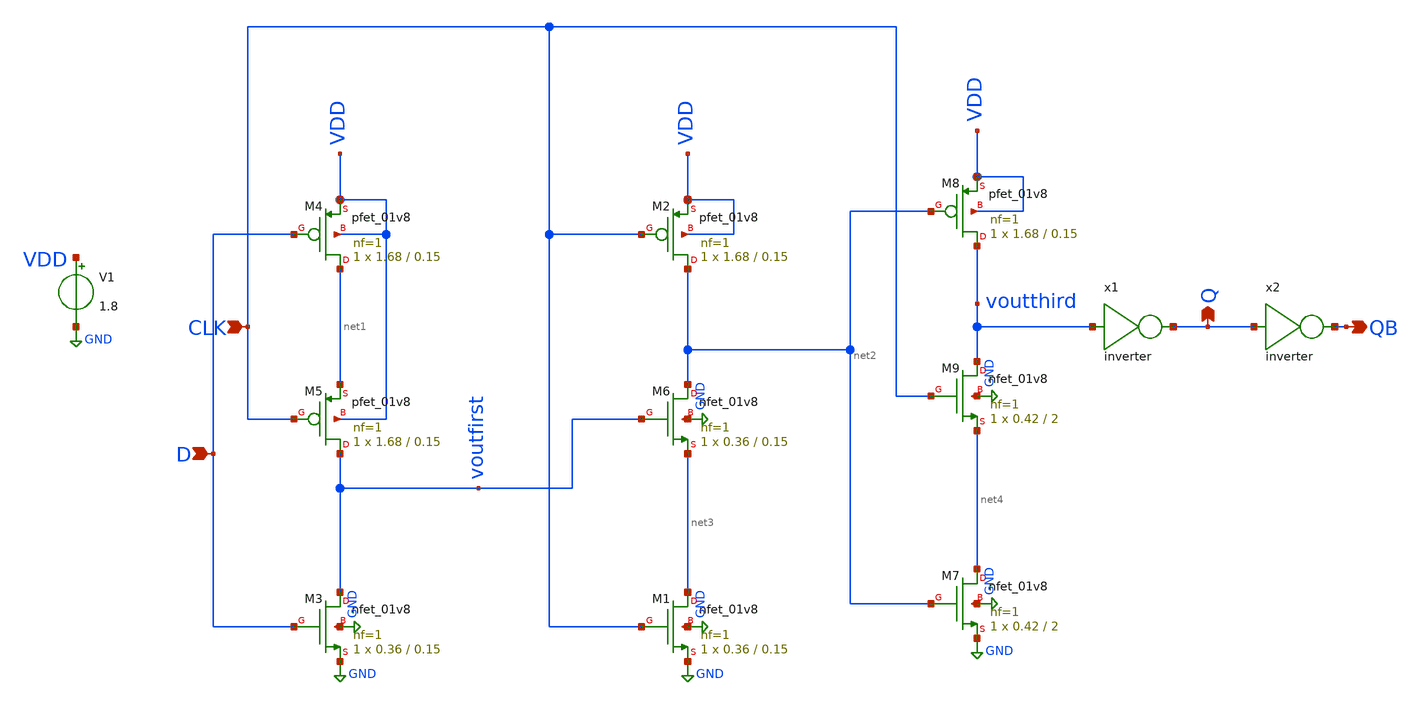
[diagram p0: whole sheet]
** sch_path: TSPC_Dff.sch
**.subckt TSPC_Dff D CLK Q QB
*.ipin D
*.ipin CLK
*.opin Q
*.opin QB
V1 VDD GND 1.8
XM3 voutfirst D GND GND sky130_fd_pr__nfet_01v8 L=0.15 W=0.36 nf=1 ad='int((nf+1)/2) * W/nf * 0.29' as='int((nf+2)/2) * W/nf * 0.29'
+ pd='2*int((nf+1)/2) * (W/nf + 0.29)' ps='2*int((nf+2)/2) * (W/nf + 0.29)' nrd='0.29 / W' nrs='0.29 / W'
+ sa=0 sb=0 sd=0 mult=1 m=1
XM4 net1 D VDD VDD sky130_fd_pr__pfet_01v8 L=0.15 W=1.68 nf=1 ad='int((nf+1)/2) * W/nf * 0.29' as='int((nf+2)/2) * W/nf * 0.29'
+ pd='2*int((nf+1)/2) * (W/nf + 0.29)' ps='2*int((nf+2)/2) * (W/nf + 0.29)' nrd='0.29 / W' nrs='0.29 / W'
+ sa=0 sb=0 sd=0 mult=1 m=1
XM5 voutfirst CLK net1 VDD sky130_fd_pr__pfet_01v8 L=0.15 W=1.68 nf=1 ad='int((nf+1)/2) * W/nf * 0.29'
+ as='int((nf+2)/2) * W/nf * 0.29' pd='2*int((nf+1)/2) * (W/nf + 0.29)' ps='2*int((nf+2)/2) * (W/nf + 0.29)'
+ nrd='0.29 / W' nrs='0.29 / W' sa=0 sb=0 sd=0 mult=1 m=1
XM1 net3 CLK GND GND sky130_fd_pr__nfet_01v8 L=0.15 W=0.36 nf=1 ad='int((nf+1)/2) * W/nf * 0.29' as='int((nf+2)/2) * W/nf * 0.29'
+ pd='2*int((nf+1)/2) * (W/nf + 0.29)' ps='2*int((nf+2)/2) * (W/nf + 0.29)' nrd='0.29 / W' nrs='0.29 / W'
+ sa=0 sb=0 sd=0 mult=1 m=1
XM2 net2 CLK VDD VDD sky130_fd_pr__pfet_01v8 L=0.15 W=1.68 nf=1 ad='int((nf+1)/2) * W/nf * 0.29' as='int((nf+2)/2) * W/nf * 0.29'
+ pd='2*int((nf+1)/2) * (W/nf + 0.29)' ps='2*int((nf+2)/2) * (W/nf + 0.29)' nrd='0.29 / W' nrs='0.29 / W'
+ sa=0 sb=0 sd=0 mult=1 m=1
XM6 net2 voutfirst net3 GND sky130_fd_pr__nfet_01v8 L=0.15 W=0.36 nf=1 ad='int((nf+1)/2) * W/nf * 0.29'
+ as='int((nf+2)/2) * W/nf * 0.29' pd='2*int((nf+1)/2) * (W/nf + 0.29)' ps='2*int((nf+2)/2) * (W/nf + 0.29)'
+ nrd='0.29 / W' nrs='0.29 / W' sa=0 sb=0 sd=0 mult=1 m=1
XM7 net4 net2 GND GND sky130_fd_pr__nfet_01v8 L=2 W=0.42 nf=1 ad='int((nf+1)/2) * W/nf * 0.29' as='int((nf+2)/2) * W/nf * 0.29'
+ pd='2*int((nf+1)/2) * (W/nf + 0.29)' ps='2*int((nf+2)/2) * (W/nf + 0.29)' nrd='0.29 / W' nrs='0.29 / W'
+ sa=0 sb=0 sd=0 mult=1 m=1
XM8 voutthird net2 VDD VDD sky130_fd_pr__pfet_01v8 L=0.15 W=1.68 nf=1 ad='int((nf+1)/2) * W/nf * 0.29'
+ as='int((nf+2)/2) * W/nf * 0.29' pd='2*int((nf+1)/2) * (W/nf + 0.29)' ps='2*int((nf+2)/2) * (W/nf + 0.29)'
+ nrd='0.29 / W' nrs='0.29 / W' sa=0 sb=0 sd=0 mult=1 m=1
XM9 voutthird CLK net4 GND sky130_fd_pr__nfet_01v8 L=2 W=0.42 nf=1 ad='int((nf+1)/2) * W/nf * 0.29' as='int((nf+2)/2) * W/nf * 0.29'
+ pd='2*int((nf+1)/2) * (W/nf + 0.29)' ps='2*int((nf+2)/2) * (W/nf + 0.29)' nrd='0.29 / W' nrs='0.29 / W'
+ sa=0 sb=0 sd=0 mult=1 m=1
x1 voutthird Q inverter
x2 Q QB inverter
**.ends

* expanding   symbol:  /home/cegrahul/Desktop/SSCS/inverter.sym # of pins=2
** sym_path: inverter.sym
** sch_path: inverter.sch
.subckt inverter vin vout
*.ipin vin
*.opin vout
XM2 vout vin net1 net1 sky130_fd_pr__pfet_01v8 L=0.15 W=1.68 nf=1 ad='int((nf+1)/2) * W/nf * 0.29' as='int((nf+2)/2) * W/nf * 0.29'
+ pd='2*int((nf+1)/2) * (W/nf + 0.29)' ps='2*int((nf+2)/2) * (W/nf + 0.29)' nrd='0.29 / W' nrs='0.29 / W'
+ sa=0 sb=0 sd=0 mult=1 m=1
XM3 vout vin GND GND sky130_fd_pr__nfet_01v8 L=0.15 W=0.36 nf=1 ad='int((nf+1)/2) * W/nf * 0.29' as='int((nf+2)/2) * W/nf * 0.29'
+ pd='2*int((nf+1)/2) * (W/nf + 0.29)' ps='2*int((nf+2)/2) * (W/nf + 0.29)' nrd='0.29 / W' nrs='0.29 / W'
+ sa=0 sb=0 sd=0 mult=1 m=1
V3 net1 GND 1.8
.ends

.GLOBAL GND
.end
